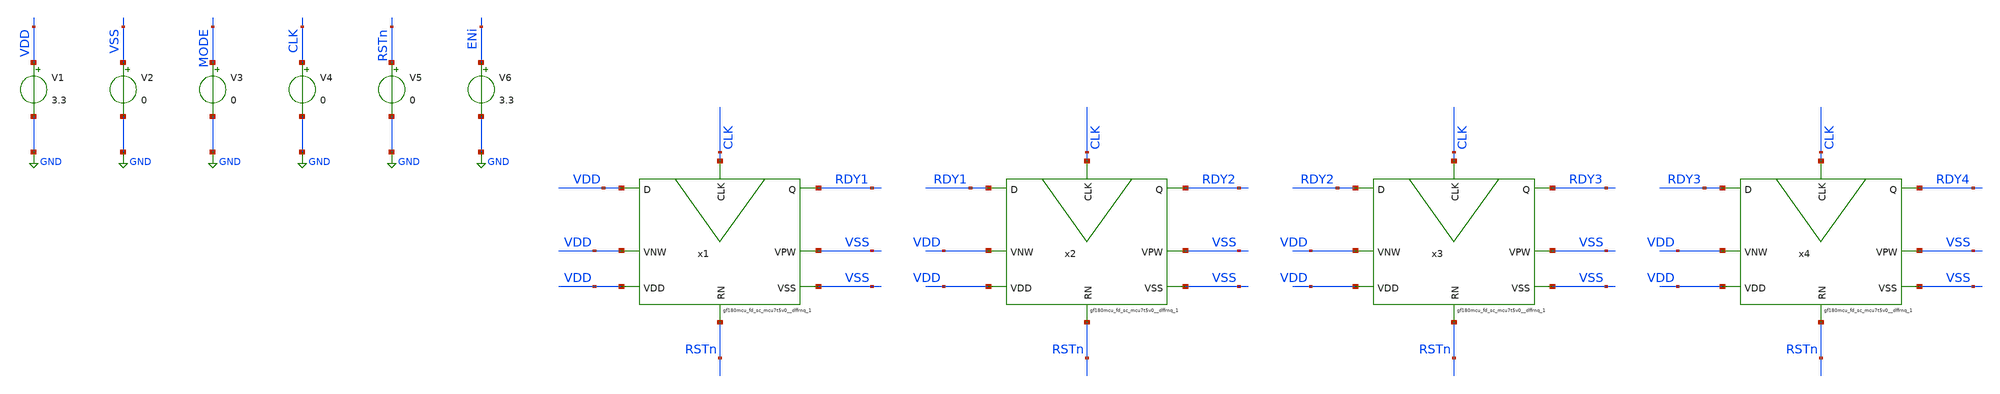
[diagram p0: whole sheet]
** sch_path: RDY/READY_sweep/READYsweep3v3.sch
**.subckt READYsweep3v3
x1 VDD RSTn CLK RDY1 VDD VDD VSS VSS gf180mcu_fd_sc_mcu7t5v0__dffrnq_1
x2 RDY1 RSTn CLK RDY2 VDD VDD VSS VSS gf180mcu_fd_sc_mcu7t5v0__dffrnq_1
x3 RDY2 RSTn CLK RDY3 VDD VDD VSS VSS gf180mcu_fd_sc_mcu7t5v0__dffrnq_1
x4 RDY3 RSTn CLK RDY4 VDD VDD VSS VSS gf180mcu_fd_sc_mcu7t5v0__dffrnq_1
V1 VDD GND 3.3
V2 VSS GND 0
V3 MODE GND 0
V4 CLK GND 0
V5 RSTn GND 0
V6 ENi GND 3.3
**** begin user architecture code

.include $::180MCU_MODELS/design.ngspice
.lib $::180MCU_MODELS/sm141064.ngspice typical



.include /foss/designs/DBSchip/dffsnq/gf180mcu_fd_sc_mcu7t5v0__dffsnq_1.spice
.include /foss/designs/DBSchip/dffrnq/gf180mcu_fd_sc_mcu7t5v0__dffrnq_1.spice
.include /foss/designs/DBSchip/and2/gf180mcu_fd_sc_mcu7t5v0__and2_1.spice
.include /foss/designs/DBSchip/or2/gf180mcu_fd_sc_mcu7t5v0__or2_1.spice
.include /foss/designs/DBSchip/nor2/gf180mcu_fd_sc_mcu7t5v0__nor2_1.spice
.include /foss/designs/DBSchip/nand3/gf180mcu_fd_sc_mcu7t5v0__nand3_1.spice
.include /foss/designs/DBSchip/inv_1/gf180mcu_fd_sc_mcu7t5v0__inv_1.spice
.include /foss/designs/DBSchip/ROW/READY_sweep/CHANNEL_sub.spice




* port order confirmed from **.subckt line of CHANNEL.spice
.subckt chan ENi MODE RSTn CLK READY SW_REC SW_IPG SW_RECb SW_IPGb VDD VSS
XD MODE RSTn CLK VDD VSS SW_REC SW_IPG SW_RECb SW_IPGb ENi READY CHANNEL
.ends
XU1 ENi MODE RSTn CLK RDY1 SW_REC1 SW_IPG1 SW_RECB1 SW_IPGB1 VDD VSS chan
XU2 ENi MODE RSTn CLK RDY2 SW_REC2 SW_IPG2 SW_RECB2 SW_IPGB2 VDD VSS chan
XU3 ENi MODE RSTn CLK RDY3 SW_REC3 SW_IPG3 SW_RECB3 SW_IPGB3 VDD VSS chan
XU4 ENi MODE RSTn CLK RDY4 SW_REC4 SW_IPG4 SW_RECB4 SW_IPGB4 VDD VSS chan
CI1 SW_IPG1 0 25f
CI2 SW_IPG2 0 25f
CI3 SW_IPG3 0 25f
CI4 SW_IPG4 0 25f
CR1 SW_REC1 0 25f
CR2 SW_REC2 0 25f
CR3 SW_REC3 0 25f
CR4 SW_REC4 0 25f



.control
save all
**
** ---- clock ----
let fclk     = 1e5
let tper_clk = 1/fclk
let tfr_clk  = 0.01*tper_clk
let ton_clk  = 0.5*tper_clk - 2*tfr_clk
let tper2clk = 0.95*tper_clk
**
** ---- resolution follows the fastest edge in the deck ----
let tmax  = tfr_clk/200
let tstep = tmax
**
let tstop = 24*tper_clk
**
** ---- MODE: square wave, 8 clock periods per half ----
let tfr    = tfr_clk
let tper_D = 16*tper_clk
let ton_D  = 0.5*tper_D - 2*tfr
**
** ---- RSTn: low for the first 2 clock periods, then high ----
let td_R = 2*tper_clk
**
alter @v4[PULSE] = [ 0 3.3 0 $&tfr_clk $&tfr_clk $&ton_clk $&tper2clk 0 ]
alter @v3[PULSE] = [ 0 3.3 0 $&tfr $&tfr $&ton_D $&tper_D 0 ]
alter @v5[PULSE] = [ 0 3.3 $&td_R $&tfr $&tfr $&tstop $&tstop 0 ]
**
op

tran $&tstep $&tstop 0 $&tmax

**
** ---- the N sweep ----
plot v(sw_ipg1) v(sw_ipg2)+6 v(sw_ipg3)+12 v(sw_ipg4)+18
**
** ---- READY against its own output, N=1 and N=4 ----
plot v(clk) v(rstn)+6 v(rdy1)+12 v(sw_ipg1)+18 v(rdy4)+24 v(sw_ipg4)+30
**
** ---- worst-case output excursion while READY is still low ----
** If maximum() is not recognised, try vecmax().
let pre1 = v(sw_ipg1) * (v(rdy1) < 2.5)
let pre2 = v(sw_ipg2) * (v(rdy2) < 2.5)
let pre3 = v(sw_ipg3) * (v(rdy3) < 2.5)
let pre4 = v(sw_ipg4) * (v(rdy4) < 2.5)
print maximum(pre1)
print maximum(pre2)
print maximum(pre3)
print maximum(pre4)
**
wrdata channel_ready_3v3_100k.txt v(clk) v(rstn) v(rdy1) v(rdy2) v(rdy3) v(rdy4)
wrdata channel_swipg_3v3_100k.txt v(clk) v(rstn) v(sw_ipg1) v(sw_ipg2) v(sw_ipg3) v(sw_ipg4)
wrdata channel_swrec_3v3_100k.txt v(clk) v(rstn) v(sw_rec1) v(sw_rec2) v(sw_rec3) v(sw_rec4)
**
write channel_ready_sweep_3v3_100k.raw
.endc



**** end user architecture code
**.ends
.GLOBAL GND
.end
